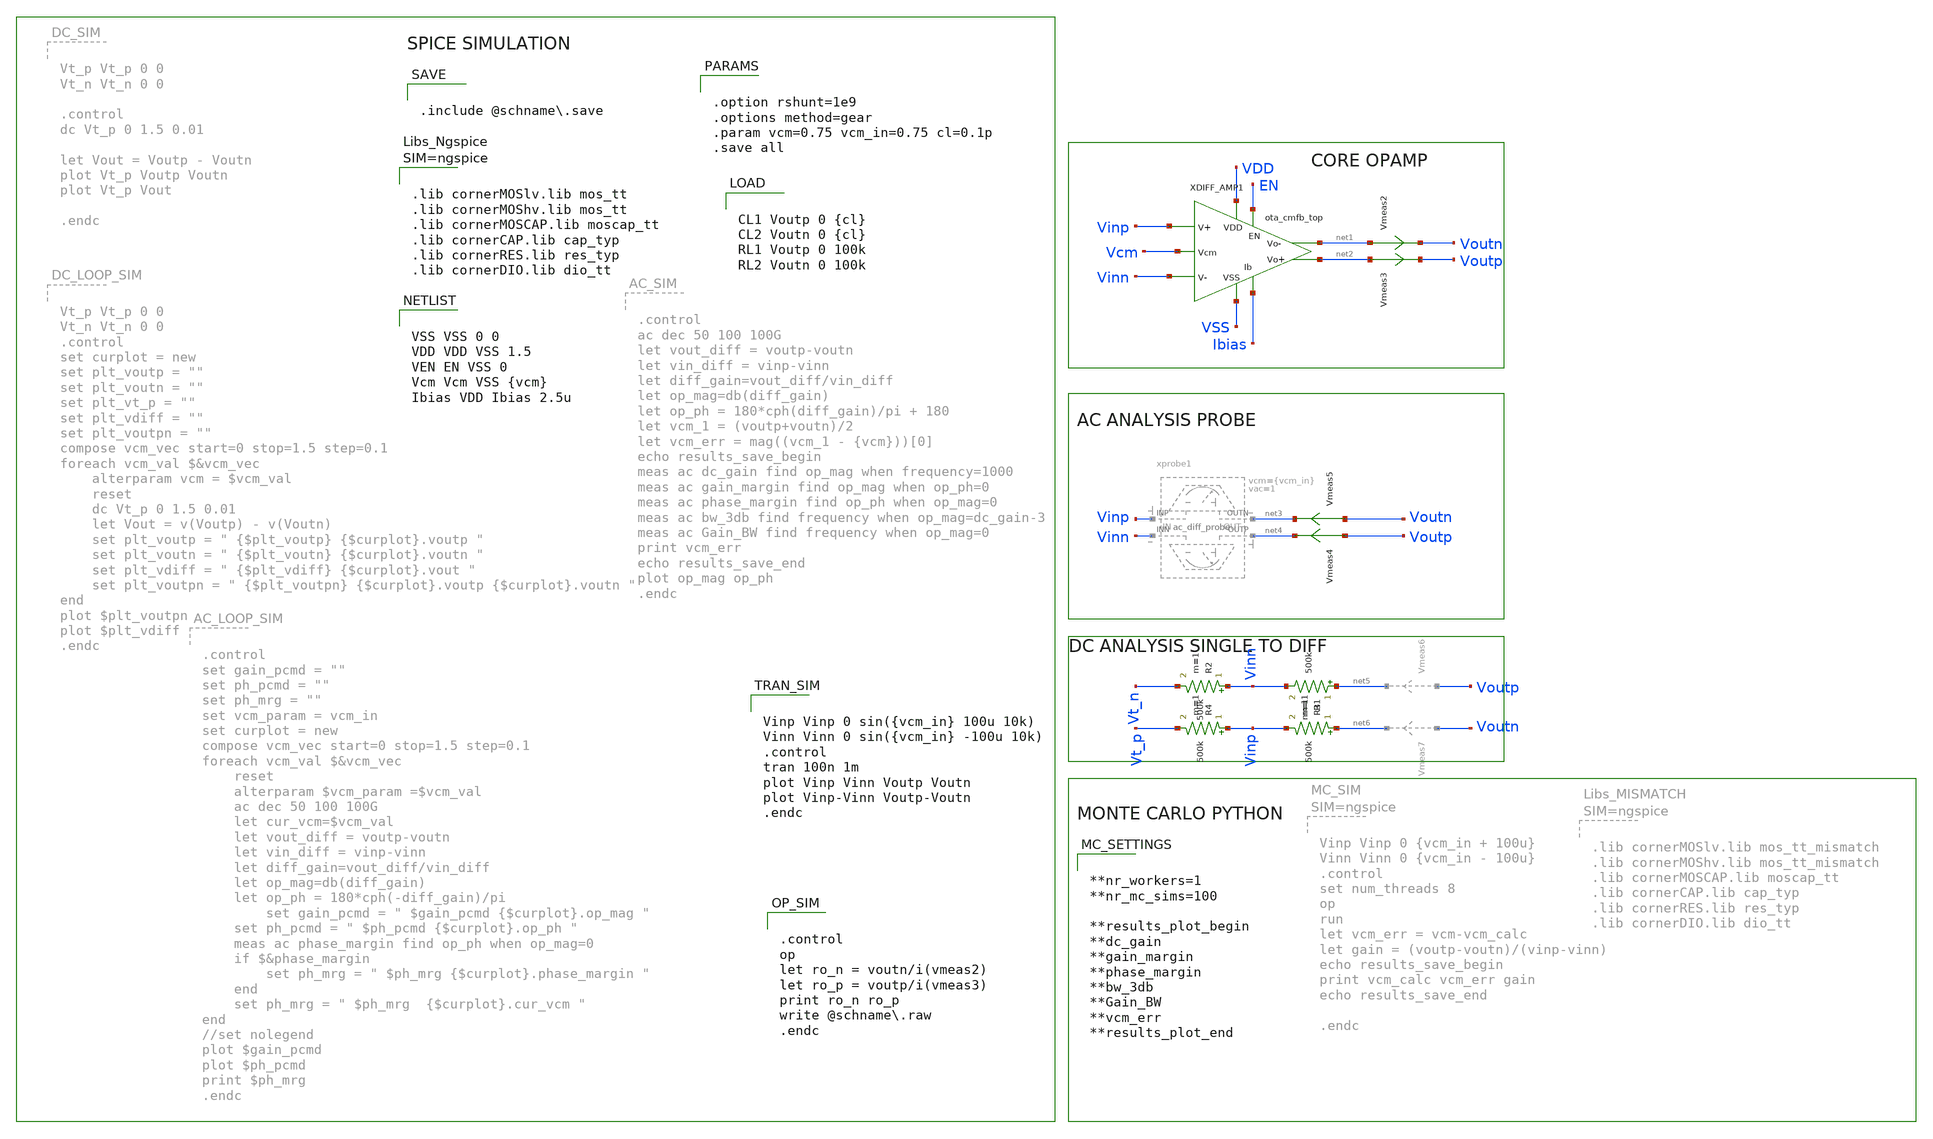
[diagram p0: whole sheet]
** sch_path: schema/ota_cmfb_top_tb.sch
**.subckt ota_cmfb_top_tb
Vmeas2 net1 Voutn 0
.save i(vmeas2)
Vmeas3 net2 Voutp 0
.save i(vmeas3)
Vmeas4 Voutp net4 0
.save i(vmeas4)
Vmeas5 Voutn net3 0
.save i(vmeas5)
R1 net5 Vinn 500k m=1
R2 Vinn Vt_n 500k m=1
R3 net6 Vinp 500k m=1
R4 Vinp Vt_p 500k m=1
XDIFF_AMP1 Vcm VDD EN Vinp net1 net2 Vinn VSS Ibias ota_cmfb_top
**** begin user architecture code


VSS VSS 0 0
VDD VDD VSS 1.5
VEN EN VSS 0
Vcm Vcm VSS {vcm}
Ibias VDD Ibias 2.5u



.control
op
let ro_n = voutn/i(vmeas2)
let ro_p = voutp/i(vmeas3)
print ro_n ro_p
write @schname.raw
.endc




.lib cornerMOSlv.lib mos_tt
.lib cornerMOShv.lib mos_tt
.lib cornerMOSCAP.lib moscap_tt
.lib cornerCAP.lib cap_typ
.lib cornerRES.lib res_typ
.lib cornerDIO.lib dio_tt





.option rshunt=1e9
.options method=gear
.param vcm=0.75 vcm_in=0.75 cl=0.1p
.save all




CL1 Voutp 0 {cl}
CL2 Voutn 0 {cl}
RL1 Voutp 0 100k
RL2 Voutn 0 100k



.include @schname.save



Vinp Vinp 0 sin({vcm_in} 100u 10k)
Vinn Vinn 0 sin({vcm_in} -100u 10k)
.control
tran 100n 1m
plot Vinp Vinn Voutp Voutn
plot Vinp-Vinn Voutp-Voutn
.endc




**nr_workers=1
**nr_mc_sims=100

**results_plot_begin
**dc_gain
**gain_margin
**phase_margin
**bw_3db
**Gain_BW
**vcm_err
**results_plot_end


**** end user architecture code
**.ends

* expanding   symbol:  ac_diff_probe/ac_diff_probe.sym # of pins=4
** sym_path: schema/ac_diff_probe/ac_diff_probe.sym
** sch_path: schema/ac_diff_probe/ac_diff_probe.sch
.subckt ac_diff_probe INP OUTN INN OUTP  vcm=0.75 vac=0.1
*.iopin OUTN
*.iopin INP
*.iopin OUTP
*.iopin INN
xprobe1 OUTN INP ac_probe vcm={vcm} vac={vac}
xprobe2 OUTP INN ac_probe vcm={vcm} vac=-{vac}
.ends


* expanding   symbol:  schema/ota_cmfb_top.sym # of pins=9
** sym_path: schema/ota_cmfb_top.sym
** sch_path: schema/ota_cmfb_top.sch
.subckt ota_cmfb_top Vcm VDD EN Vinp Voutn Voutp Vinn VSS Ibias
*.iopin VDD
*.ipin Vinn
*.ipin Vinp
*.ipin Ibias
*.opin Voutn
*.opin Voutp
*.iopin VSS
*.ipin EN
*.ipin Vcm
xopamp1 VDD Vcm_reg Vinn Vinp Ibias Voutn Voutp VSS EN Vbias ota_cmfb_core
xota1 VDD EN Vbias Vcm_calc Vcm Vcm_reg VSS ota_cmfb_fbota
XM7 VSS VSS Vbias VSS sg13_lv_nmos w=0.25u l=0.5u ng=1 m=2 mm_ok=1
XR1 Voutn Vcm_calc VSS rhigh w=0.5e-6 l=1e-6*10 m=1 b=0 mm_ok=1
XR2 Voutp Vcm_calc VSS rhigh w=0.5e-6 l=1e-6*10 m=1 b=0 mm_ok=1
XM1 VSS VSS VSS VSS sg13_lv_nmos w=3.2u l=0.5u ng=1 m=10 mm_ok=1
XM2 VDD VDD VDD VDD sg13_lv_pmos w=1.985u l=0.5u ng=1 m=100 mm_ok=1
XD1 VSS EN dantenna l=0.78u w=0.78u
XD2 EN VDD dpantenna l=1.34u w=1.05u
.ends


* expanding   symbol:  ac_probe/ac_probe.sym # of pins=2
** sym_path: schema/ac_probe/ac_probe.sym
** sch_path: schema/ac_probe/ac_probe.sch
.subckt ac_probe OUT IN  vcm=0.75 vac=0.01

*.iopin IN
*.iopin OUT
C1 0 IN 1 m=1
V1 IN 0 {vcm} ac {vac}
R1 OUT IN 1G m=1
.ends


* expanding   symbol:  ota_cmfb_core/ota_cmfb_core.sym # of pins=10
** sym_path: schema/ota_cmfb_core/ota_cmfb_core.sym
** sch_path: schema/ota_cmfb_core/ota_cmfb_core.sch
.subckt ota_cmfb_core VDD Vcm_reg Vinn Vinp Ibias Voutn Voutp VSS EN Vbias
*.opin Voutn
*.opin Voutp
*.iopin VDD
*.iopin VSS
*.ipin Vinp
*.ipin Ibias
*.ipin Vinn
*.ipin Vcm_reg
*.ipin EN
*.opin Vbias
XMD Voutp_st1 Vbias VSS VSS sg13_lv_nmos w=0.25u l=10u ng=1 m=8 mm_ok=1
XMB src_ab Vinn Voutp_st1 VDD sg13_lv_pmos w=2.5u l=2u ng=1 m=8 mm_ok=1
XMC Voutn_st1 Vbias VSS VSS sg13_lv_nmos w=0.25u l=10u ng=1 m=8 mm_ok=1
XMA src_ab Vinp Voutn_st1 VDD sg13_lv_pmos w=2.5u l=2u ng=1 m=8 mm_ok=1
XMM VDD Vcm_reg src_ab VDD sg13_lv_pmos w=2.5u l=10u ng=1 m=8 mm_ok=1
XME Vbias Vbias VSS VSS sg13_lv_nmos w=0.25u l=10u ng=1 m=2 mm_ok=1
xsf1 VDD Voutn_st1 Voutp Vbias VSS EN ota_cmfb_core_push_pull_output_stage
xsf2 VDD Voutp_st1 Voutn Vbias VSS EN ota_cmfb_core_push_pull_output_stage
XMN0 EN_N EN VSS VSS sg13_lv_nmos w=2.96u l=130.00n ng=1 m=1 mm_ok=1
XMP0 EN_N EN VDD VDD sg13_lv_pmos w=4.48u l=130.00n ng=1 m=1 mm_ok=1
XMN1 Vbias EN_N VSS VSS sg13_lv_nmos w=740.00n l=130.00n ng=1 m=1 mm_ok=1
XMP1 Vcm_reg EN VDD VDD sg13_lv_pmos w=150.00n l=130.00n ng=1 m=1 mm_ok=1
XMB1 VDD VDD src_ab VDD sg13_lv_pmos w=2.5u l=0.5u ng=1 m=4 mm_ok=1
XMN2 Ibias EN Vbias VSS sg13_lv_nmos w=740.00n l=130.00n ng=1 m=1 mm_ok=1
.ends


* expanding   symbol:  ota_cmfb_fbota/ota_cmfb_fbota.sym # of pins=7
** sym_path: schema/ota_cmfb_fbota/ota_cmfb_fbota.sym
** sch_path: schema/ota_cmfb_fbota/ota_cmfb_fbota.sch
.subckt ota_cmfb_fbota VDD EN Ibias Vinn Vinp Vout VSS
*.opin Vout
*.iopin VDD
*.iopin VSS
*.ipin Vinp
*.ipin Ibias
*.ipin Vinn
*.ipin EN
XMJ Vout mirror VSS VSS sg13_lv_nmos w=0.25u l=10u ng=1 m=4 mm_ok=1
XML Vout Vinn src_kl VDD sg13_lv_pmos w=2.5u l=2u ng=1 m=2 mm_ok=1
XMI mirror mirror VSS VSS sg13_lv_nmos w=0.25u l=10u ng=1 m=4 mm_ok=1
XMK mirror Vinp src_kl VDD sg13_lv_pmos w=2.5u l=2u ng=1 m=2 mm_ok=1
XMO src_kl tail_bias VDD VDD sg13_lv_pmos w=1.25u l=5u ng=1 m=8 mm_ok=1
XMN VDD tail_bias tail_bias VDD sg13_lv_pmos w=1.25u l=5u ng=1 m=2 mm_ok=1
XMH tail_bias Ibias VSS VSS sg13_lv_nmos w=0.25u l=10u ng=1 m=2 mm_ok=1
XMN1 mirror EN_N VSS VSS sg13_lv_nmos w=740.00n l=130.00n ng=1 m=1 mm_ok=1
XM2 VSS VSS tail_bias VSS sg13_lv_nmos w=0.25u l=0.5u ng=1 m=2 mm_ok=1
XMK1 mirror VDD VDD VDD sg13_lv_pmos w=2.5u l=0.5u ng=1 m=1 mm_ok=1
XMK2 Vout VDD VDD VDD sg13_lv_pmos w=2.5u l=0.5u ng=1 m=1 mm_ok=1
XMK3 src_kl VDD VDD VDD sg13_lv_pmos w=2.5u l=0.5u ng=1 m=2 mm_ok=1
XMK4 tail_bias VDD VDD VDD sg13_lv_pmos w=1.25u l=0.5u ng=1 m=2 mm_ok=1
XMN0 EN_N EN VSS VSS sg13_lv_nmos w=2.96u l=130.00n ng=1 m=1 mm_ok=1
XMP0 EN_N EN VDD VDD sg13_lv_pmos w=4.48u l=130.00n ng=1 m=1 mm_ok=1
XMP1 tail_bias EN VDD VDD sg13_lv_pmos w=150.00n l=130.00n ng=1 m=1 mm_ok=1
.ends


* expanding   symbol:  ota_cmfb_core/ota_cmfb_core_push_pull_output_stage.sym # of pins=6
** sym_path: schema/ota_cmfb_core/ota_cmfb_core_push_pull_output_stage.sym
** sch_path: schema/ota_cmfb_core/ota_cmfb_core_push_pull_output_stage.sch
.subckt ota_cmfb_core_push_pull_output_stage VDD Vin Vout Vbias VSS EN
*.iopin VSS
*.iopin VDD
*.ipin Vbias
*.ipin Vin
*.opin Vout
*.ipin EN
XM1 Vout Vin_shifted VSS VSS sg13_lv_nmos w=0.5u l=10u ng=1 m=1 mm_ok=1
XM2 VDD Vin Vout VDD sg13_lv_pmos w=5u l=0.5u ng=1 m=1 mm_ok=1
XMC VDD Vbiasp CD_DRN VDD sg13_lv_pmos w=2.5u l=3u ng=1 m=4 mm_ok=1
XME Vin_shifted Vcasp2 Vin VDD sg13_lv_pmos w=2.5u l=3u ng=1 m=2 mm_ok=1
XMD CD_DRN Vcasp Vin VDD sg13_lv_pmos w=2.5u l=3u ng=1 m=4 mm_ok=1
XMN Vin Vcasn2 Vin_shifted VSS sg13_lv_nmos w=0.7u l=3u ng=1 m=2 mm_ok=1
XMH VDD Vbiasp net1 VDD sg13_lv_pmos w=2.5u l=3u ng=1 m=4 mm_ok=1
XMI net1 Vcasp Vcasp VDD sg13_lv_pmos w=2.5u l=3u ng=1 m=4 mm_ok=1
XMJ Vcasp Vcasp2 Vcasp2 VDD sg13_lv_pmos w=2.5u l=3u ng=1 m=4 mm_ok=1
XMB VDD Vbiasp Vcasn2 VDD sg13_lv_pmos w=2.5u l=3u ng=1 m=4 mm_ok=1
XMO Vcasn2 Vcasn2 Vcasn VSS sg13_lv_nmos w=0.7u l=3u ng=1 m=4 mm_ok=1
XR1 net2 Vout VSS rhigh w=0.5e-6 l=1e-6*8 m=1 b=0 mm_ok=1
XC1 Vin net2 sg13_moscap_p w=3.5u l=21.5u m=1 mm_ok=1
XMFG Vbiasp Vbias VSS VSS sg13_lv_nmos w=0.25u l=10u ng=1 m=2 mm_ok=1
XMA VDD Vbiasp Vbiasp VDD sg13_lv_pmos w=2.5u l=3u ng=1 m=10 mm_ok=1
XMP Vcasn Vcasn Vbiasn VSS sg13_lv_nmos w=0.7u l=3u ng=1 m=4 mm_ok=1
XMQ Vbiasn Vbiasn VSS VSS sg13_lv_nmos w=0.7u l=3u ng=1 m=4 mm_ok=1
XMM Vin_shifted Vcasn src_ml VSS sg13_lv_nmos w=0.7u l=3u ng=1 m=4 mm_ok=1
XML src_ml Vbiasn VSS VSS sg13_lv_nmos w=0.7u l=3u ng=1 m=4 mm_ok=1
XMK Vcasp2 Vbiasn VSS VSS sg13_lv_nmos w=0.7u l=3u ng=1 m=4 mm_ok=1
XM3 CD_DRN VDD VDD VDD sg13_lv_pmos w=2.5u l=0.5u ng=1 m=2 mm_ok=1
XM4 Vin_shifted VDD VDD VDD sg13_lv_pmos w=2.5u l=0.5u ng=1 m=1 mm_ok=1
XM5 Vbiasp VDD VDD VDD sg13_lv_pmos w=2.5u l=0.5u ng=1 m=1 mm_ok=1
XM6 Vin VDD VDD VDD sg13_lv_pmos w=2.5u l=0.5u ng=1 m=1 mm_ok=1
XM7 VSS VSS Vin_shifted VSS sg13_lv_nmos w=0.7u l=0.5u ng=1 m=2 mm_ok=1
XM8 VSS VSS Vcasn VSS sg13_lv_nmos w=0.7u l=0.5u ng=1 m=4 mm_ok=1
XMX VSS VSS Vin_shifted VSS sg13_lv_nmos w=0.7u l=3u ng=1 m=4 mm_ok=1
XM9 VSS VSS src_ml VSS sg13_lv_nmos w=0.7u l=0.5u ng=1 m=4 mm_ok=1
XM10 Vcasp VDD VDD VDD sg13_lv_pmos w=2.5u l=0.5u ng=1 m=2 mm_ok=1
XM12 VSS VSS Vbiasp VSS sg13_lv_nmos w=0.25u l=0.5u ng=1 m=2 mm_ok=1
XM13 Vbiasp EN VDD VDD sg13_lv_pmos w=0.15u l=0.13u ng=1 m=1 mm_ok=1
XMN0 EN_N EN VSS VSS sg13_lv_nmos w=2.96u l=130.00n ng=1 m=1 mm_ok=1
XMP0 EN_N EN VDD VDD sg13_lv_pmos w=4.48u l=130.00n ng=1 m=1 mm_ok=1
XMN1 Vbiasn EN_N VSS VSS sg13_lv_nmos w=740.00n l=130.00n ng=1 m=1 mm_ok=1
XM14 Vin EN VDD VDD sg13_lv_pmos w=0.15u l=0.13u ng=1 m=1 mm_ok=1
.ends

.end
